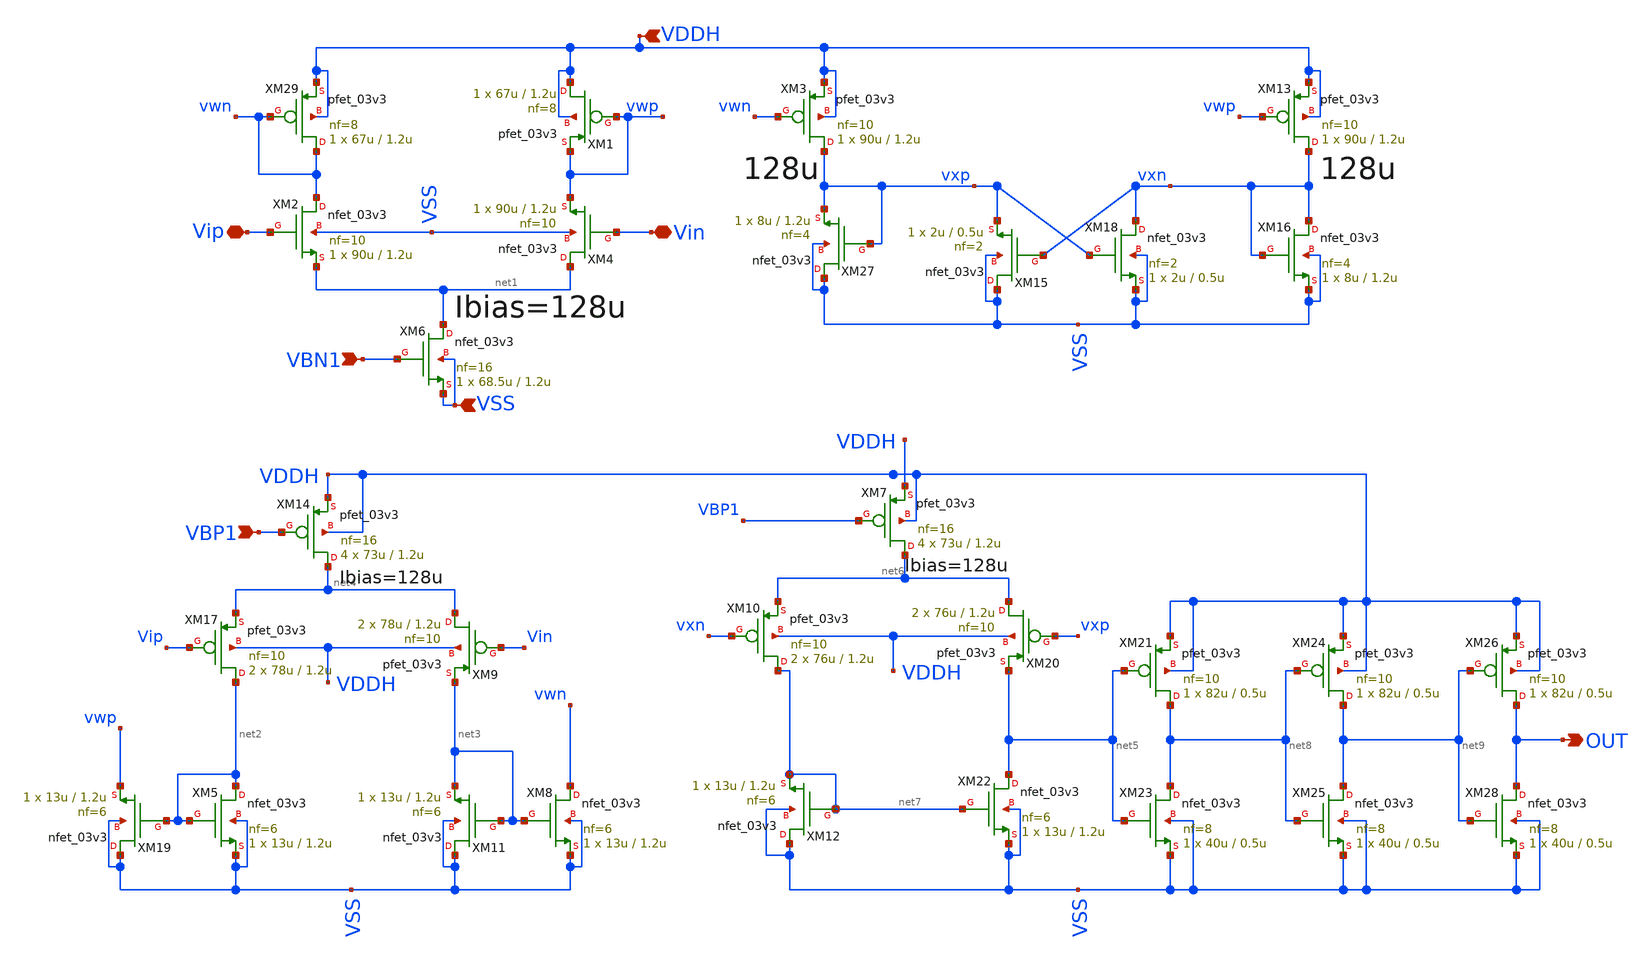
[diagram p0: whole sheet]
** sch_path: Schematics/COMPARADOR/comparator_3v3_VSS.sch
**.subckt comparator_3v3_VSS Vip Vin VDDH VBN1 VBP1 OUT VSS
*.iopin Vip
*.iopin Vin
*.ipin VDDH
*.ipin VBN1
*.ipin VBP1
*.opin OUT
*.ipin VSS
XM2 vwn Vip net1 VSS nfet_03v3 L=1.2u W=90u nf=10 ad='int((nf+1)/2) * W/nf * 0.18u' as='int((nf+2)/2) * W/nf * 0.18u'
+ pd='2*int((nf+1)/2) * (W/nf + 0.18u)' ps='2*int((nf+2)/2) * (W/nf + 0.18u)' nrd='0.18u / W' nrs='0.18u / W'
+ sa=0 sb=0 sd=0 m=1
XM4 net1 Vin vwp VSS nfet_03v3 L=1.2u W=90u nf=10 ad='int((nf+1)/2) * W/nf * 0.18u' as='int((nf+2)/2) * W/nf * 0.18u'
+ pd='2*int((nf+1)/2) * (W/nf + 0.18u)' ps='2*int((nf+2)/2) * (W/nf + 0.18u)' nrd='0.18u / W' nrs='0.18u / W'
+ sa=0 sb=0 sd=0 m=1
XM29 vwn vwn VDDH VDDH pfet_03v3 L=1.2u W=67u nf=8 ad='int((nf+1)/2) * W/nf * 0.18u' as='int((nf+2)/2) * W/nf * 0.18u'
+ pd='2*int((nf+1)/2) * (W/nf + 0.18u)' ps='2*int((nf+2)/2) * (W/nf + 0.18u)' nrd='0.18u / W' nrs='0.18u / W'
+ sa=0 sb=0 sd=0 m=1
XM1 VDDH vwp vwp VDDH pfet_03v3 L=1.2u W=67u nf=8 ad='int((nf+1)/2) * W/nf * 0.18u' as='int((nf+2)/2) * W/nf * 0.18u'
+ pd='2*int((nf+1)/2) * (W/nf + 0.18u)' ps='2*int((nf+2)/2) * (W/nf + 0.18u)' nrd='0.18u / W' nrs='0.18u / W'
+ sa=0 sb=0 sd=0 m=1
XM6 net1 VBN1 VSS VSS nfet_03v3 L=1.2u W=68.5u nf=16 ad='int((nf+1)/2) * W/nf * 0.18u' as='int((nf+2)/2) * W/nf * 0.18u'
+ pd='2*int((nf+1)/2) * (W/nf + 0.18u)' ps='2*int((nf+2)/2) * (W/nf + 0.18u)' nrd='0.18u / W' nrs='0.18u / W'
+ sa=0 sb=0 sd=0 m=1
XM3 vxp vwn VDDH VDDH pfet_03v3 L=1.2u W=90u nf=10 ad='int((nf+1)/2) * W/nf * 0.18u' as='int((nf+2)/2) * W/nf * 0.18u'
+ pd='2*int((nf+1)/2) * (W/nf + 0.18u)' ps='2*int((nf+2)/2) * (W/nf + 0.18u)' nrd='0.18u / W' nrs='0.18u / W'
+ sa=0 sb=0 sd=0 m=1
XM13 vxn vwp VDDH VDDH pfet_03v3 L=1.2u W=90u nf=10 ad='int((nf+1)/2) * W/nf * 0.18u' as='int((nf+2)/2) * W/nf * 0.18u'
+ pd='2*int((nf+1)/2) * (W/nf + 0.18u)' ps='2*int((nf+2)/2) * (W/nf + 0.18u)' nrd='0.18u / W' nrs='0.18u / W'
+ sa=0 sb=0 sd=0 m=1
XM27 VSS vxp vxp VSS nfet_03v3 L=1.2u W=8u nf=4 ad='int((nf+1)/2) * W/nf * 0.18u' as='int((nf+2)/2) * W/nf * 0.18u'
+ pd='2*int((nf+1)/2) * (W/nf + 0.18u)' ps='2*int((nf+2)/2) * (W/nf + 0.18u)' nrd='0.18u / W' nrs='0.18u / W'
+ sa=0 sb=0 sd=0 m=1
XM16 vxn vxn VSS VSS nfet_03v3 L=1.2u W=8u nf=4 ad='int((nf+1)/2) * W/nf * 0.18u' as='int((nf+2)/2) * W/nf * 0.18u'
+ pd='2*int((nf+1)/2) * (W/nf + 0.18u)' ps='2*int((nf+2)/2) * (W/nf + 0.18u)' nrd='0.18u / W' nrs='0.18u / W'
+ sa=0 sb=0 sd=0 m=1
XM15 VSS vxn vxp VSS nfet_03v3 L=0.5u W=2u nf=2 ad='int((nf+1)/2) * W/nf * 0.18u' as='int((nf+2)/2) * W/nf * 0.18u'
+ pd='2*int((nf+1)/2) * (W/nf + 0.18u)' ps='2*int((nf+2)/2) * (W/nf + 0.18u)' nrd='0.18u / W' nrs='0.18u / W'
+ sa=0 sb=0 sd=0 m=1
XM18 vxn vxp VSS VSS nfet_03v3 L=0.5u W=2u nf=2 ad='int((nf+1)/2) * W/nf * 0.18u' as='int((nf+2)/2) * W/nf * 0.18u'
+ pd='2*int((nf+1)/2) * (W/nf + 0.18u)' ps='2*int((nf+2)/2) * (W/nf + 0.18u)' nrd='0.18u / W' nrs='0.18u / W'
+ sa=0 sb=0 sd=0 m=1
XM14 net4 VBP1 VDDH VDDH pfet_03v3 L=1.2u W=73u nf=16 ad='int((nf+1)/2) * W/nf * 0.18u' as='int((nf+2)/2) * W/nf * 0.18u'
+ pd='2*int((nf+1)/2) * (W/nf + 0.18u)' ps='2*int((nf+2)/2) * (W/nf + 0.18u)' nrd='0.18u / W' nrs='0.18u / W'
+ sa=0 sb=0 sd=0 m=4
XM7 net6 VBP1 VDDH VDDH pfet_03v3 L=1.2u W=73u nf=16 ad='int((nf+1)/2) * W/nf * 0.18u' as='int((nf+2)/2) * W/nf * 0.18u'
+ pd='2*int((nf+1)/2) * (W/nf + 0.18u)' ps='2*int((nf+2)/2) * (W/nf + 0.18u)' nrd='0.18u / W' nrs='0.18u / W'
+ sa=0 sb=0 sd=0 m=4
XM17 net2 Vip net4 VDDH pfet_03v3 L=1.2u W=78u nf=10 ad='int((nf+1)/2) * W/nf * 0.18u' as='int((nf+2)/2) * W/nf * 0.18u'
+ pd='2*int((nf+1)/2) * (W/nf + 0.18u)' ps='2*int((nf+2)/2) * (W/nf + 0.18u)' nrd='0.18u / W' nrs='0.18u / W'
+ sa=0 sb=0 sd=0 m=2
XM9 net4 Vin net3 VDDH pfet_03v3 L=1.2u W=78u nf=10 ad='int((nf+1)/2) * W/nf * 0.18u' as='int((nf+2)/2) * W/nf * 0.18u'
+ pd='2*int((nf+1)/2) * (W/nf + 0.18u)' ps='2*int((nf+2)/2) * (W/nf + 0.18u)' nrd='0.18u / W' nrs='0.18u / W'
+ sa=0 sb=0 sd=0 m=2
XM10 net7 vxn net6 VDDH pfet_03v3 L=1.2u W=76u nf=10 ad='int((nf+1)/2) * W/nf * 0.18u' as='int((nf+2)/2) * W/nf * 0.18u'
+ pd='2*int((nf+1)/2) * (W/nf + 0.18u)' ps='2*int((nf+2)/2) * (W/nf + 0.18u)' nrd='0.18u / W' nrs='0.18u / W'
+ sa=0 sb=0 sd=0 m=2
XM20 net6 vxp net5 VDDH pfet_03v3 L=1.2u W=76u nf=10 ad='int((nf+1)/2) * W/nf * 0.18u' as='int((nf+2)/2) * W/nf * 0.18u'
+ pd='2*int((nf+1)/2) * (W/nf + 0.18u)' ps='2*int((nf+2)/2) * (W/nf + 0.18u)' nrd='0.18u / W' nrs='0.18u / W'
+ sa=0 sb=0 sd=0 m=2
XM19 VSS net2 vwp VSS nfet_03v3 L=1.2u W=13u nf=6 ad='int((nf+1)/2) * W/nf * 0.18u' as='int((nf+2)/2) * W/nf * 0.18u'
+ pd='2*int((nf+1)/2) * (W/nf + 0.18u)' ps='2*int((nf+2)/2) * (W/nf + 0.18u)' nrd='0.18u / W' nrs='0.18u / W'
+ sa=0 sb=0 sd=0 m=1
XM11 VSS net3 net3 VSS nfet_03v3 L=1.2u W=13u nf=6 ad='int((nf+1)/2) * W/nf * 0.18u' as='int((nf+2)/2) * W/nf * 0.18u'
+ pd='2*int((nf+1)/2) * (W/nf + 0.18u)' ps='2*int((nf+2)/2) * (W/nf + 0.18u)' nrd='0.18u / W' nrs='0.18u / W'
+ sa=0 sb=0 sd=0 m=1
XM8 vwn net3 VSS VSS nfet_03v3 L=1.2u W=13u nf=6 ad='int((nf+1)/2) * W/nf * 0.18u' as='int((nf+2)/2) * W/nf * 0.18u'
+ pd='2*int((nf+1)/2) * (W/nf + 0.18u)' ps='2*int((nf+2)/2) * (W/nf + 0.18u)' nrd='0.18u / W' nrs='0.18u / W'
+ sa=0 sb=0 sd=0 m=1
XM12 VSS net7 net7 VSS nfet_03v3 L=1.2u W=13u nf=6 ad='int((nf+1)/2) * W/nf * 0.18u' as='int((nf+2)/2) * W/nf * 0.18u'
+ pd='2*int((nf+1)/2) * (W/nf + 0.18u)' ps='2*int((nf+2)/2) * (W/nf + 0.18u)' nrd='0.18u / W' nrs='0.18u / W'
+ sa=0 sb=0 sd=0 m=1
XM22 net5 net7 VSS VSS nfet_03v3 L=1.2u W=13u nf=6 ad='int((nf+1)/2) * W/nf * 0.18u' as='int((nf+2)/2) * W/nf * 0.18u'
+ pd='2*int((nf+1)/2) * (W/nf + 0.18u)' ps='2*int((nf+2)/2) * (W/nf + 0.18u)' nrd='0.18u / W' nrs='0.18u / W'
+ sa=0 sb=0 sd=0 m=1
XM5 net2 net2 VSS VSS nfet_03v3 L=1.2u W=13u nf=6 ad='int((nf+1)/2) * W/nf * 0.18u' as='int((nf+2)/2) * W/nf * 0.18u'
+ pd='2*int((nf+1)/2) * (W/nf + 0.18u)' ps='2*int((nf+2)/2) * (W/nf + 0.18u)' nrd='0.18u / W' nrs='0.18u / W'
+ sa=0 sb=0 sd=0 m=1
XM21 net8 net5 VDDH VDDH pfet_03v3 L=0.5u W=82u nf=10 ad='int((nf+1)/2) * W/nf * 0.18u' as='int((nf+2)/2) * W/nf * 0.18u'
+ pd='2*int((nf+1)/2) * (W/nf + 0.18u)' ps='2*int((nf+2)/2) * (W/nf + 0.18u)' nrd='0.18u / W' nrs='0.18u / W'
+ sa=0 sb=0 sd=0 m=1
XM24 net9 net8 VDDH VDDH pfet_03v3 L=0.5u W=82u nf=10 ad='int((nf+1)/2) * W/nf * 0.18u' as='int((nf+2)/2) * W/nf * 0.18u'
+ pd='2*int((nf+1)/2) * (W/nf + 0.18u)' ps='2*int((nf+2)/2) * (W/nf + 0.18u)' nrd='0.18u / W' nrs='0.18u / W'
+ sa=0 sb=0 sd=0 m=1
XM26 OUT net9 VDDH VDDH pfet_03v3 L=0.5u W=82u nf=10 ad='int((nf+1)/2) * W/nf * 0.18u' as='int((nf+2)/2) * W/nf * 0.18u'
+ pd='2*int((nf+1)/2) * (W/nf + 0.18u)' ps='2*int((nf+2)/2) * (W/nf + 0.18u)' nrd='0.18u / W' nrs='0.18u / W'
+ sa=0 sb=0 sd=0 m=1
XM23 net8 net5 VSS VSS nfet_03v3 L=0.5u W=40u nf=8 ad='int((nf+1)/2) * W/nf * 0.18u' as='int((nf+2)/2) * W/nf * 0.18u'
+ pd='2*int((nf+1)/2) * (W/nf + 0.18u)' ps='2*int((nf+2)/2) * (W/nf + 0.18u)' nrd='0.18u / W' nrs='0.18u / W'
+ sa=0 sb=0 sd=0 m=1
XM25 net9 net8 VSS VSS nfet_03v3 L=0.5u W=40u nf=8 ad='int((nf+1)/2) * W/nf * 0.18u' as='int((nf+2)/2) * W/nf * 0.18u'
+ pd='2*int((nf+1)/2) * (W/nf + 0.18u)' ps='2*int((nf+2)/2) * (W/nf + 0.18u)' nrd='0.18u / W' nrs='0.18u / W'
+ sa=0 sb=0 sd=0 m=1
XM28 OUT net9 VSS VSS nfet_03v3 L=0.5u W=40u nf=8 ad='int((nf+1)/2) * W/nf * 0.18u' as='int((nf+2)/2) * W/nf * 0.18u'
+ pd='2*int((nf+1)/2) * (W/nf + 0.18u)' ps='2*int((nf+2)/2) * (W/nf + 0.18u)' nrd='0.18u / W' nrs='0.18u / W'
+ sa=0 sb=0 sd=0 m=1
**.ends
.end
